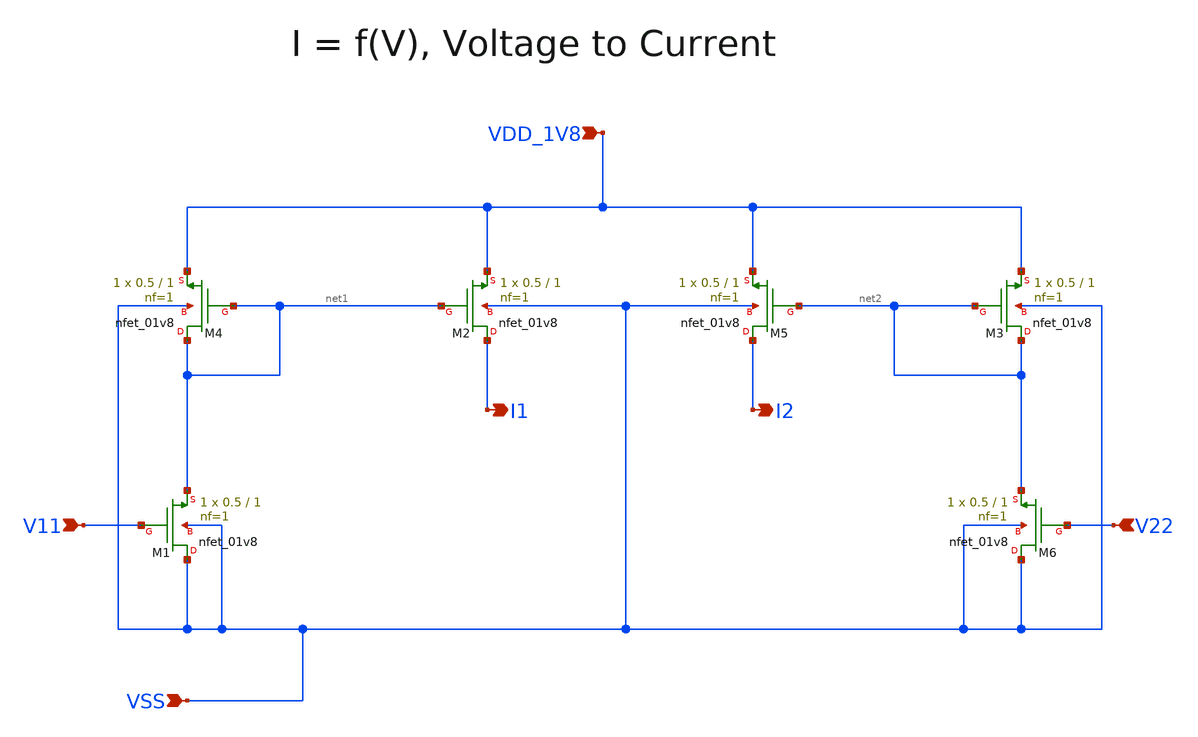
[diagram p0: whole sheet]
** sch_path: design/CNR_GR06_SKY130NM/CNR_GR06_V_to_I.sch
**.subckt CNR_GR06_V_to_I VDD_1V8 VSS I1 I2 V11 V22
*.ipin VDD_1V8
*.ipin VSS
*.opin I1
*.opin I2
*.ipin V11
*.ipin V22
XM1 VSS V11 net1 VSS sky130_fd_pr__nfet_01v8 L=1 W=0.5 nf=1 ad='int((nf+1)/2) * W/nf * 0.29' as='int((nf+2)/2) * W/nf * 0.29'
+ pd='2*int((nf+1)/2) * (W/nf + 0.29)' ps='2*int((nf+2)/2) * (W/nf + 0.29)' nrd='0.29 / W' nrs='0.29 / W'
+ sa=0 sb=0 sd=0 mult=1 m=1
XM2 I1 net1 VDD_1V8 VSS sky130_fd_pr__nfet_01v8 L=1 W=0.5 nf=1 ad='int((nf+1)/2) * W/nf * 0.29' as='int((nf+2)/2) * W/nf * 0.29'
+ pd='2*int((nf+1)/2) * (W/nf + 0.29)' ps='2*int((nf+2)/2) * (W/nf + 0.29)' nrd='0.29 / W' nrs='0.29 / W'
+ sa=0 sb=0 sd=0 mult=1 m=1
XM3 net2 net2 VDD_1V8 VSS sky130_fd_pr__nfet_01v8 L=1 W=0.5 nf=1 ad='int((nf+1)/2) * W/nf * 0.29' as='int((nf+2)/2) * W/nf * 0.29'
+ pd='2*int((nf+1)/2) * (W/nf + 0.29)' ps='2*int((nf+2)/2) * (W/nf + 0.29)' nrd='0.29 / W' nrs='0.29 / W'
+ sa=0 sb=0 sd=0 mult=1 m=1
XM4 net1 net1 VDD_1V8 VSS sky130_fd_pr__nfet_01v8 L=1 W=0.5 nf=1 ad='int((nf+1)/2) * W/nf * 0.29' as='int((nf+2)/2) * W/nf * 0.29'
+ pd='2*int((nf+1)/2) * (W/nf + 0.29)' ps='2*int((nf+2)/2) * (W/nf + 0.29)' nrd='0.29 / W' nrs='0.29 / W'
+ sa=0 sb=0 sd=0 mult=1 m=1
XM5 I2 net2 VDD_1V8 VSS sky130_fd_pr__nfet_01v8 L=1 W=0.5 nf=1 ad='int((nf+1)/2) * W/nf * 0.29' as='int((nf+2)/2) * W/nf * 0.29'
+ pd='2*int((nf+1)/2) * (W/nf + 0.29)' ps='2*int((nf+2)/2) * (W/nf + 0.29)' nrd='0.29 / W' nrs='0.29 / W'
+ sa=0 sb=0 sd=0 mult=1 m=1
XM6 VSS V22 net2 VSS sky130_fd_pr__nfet_01v8 L=1 W=0.5 nf=1 ad='int((nf+1)/2) * W/nf * 0.29' as='int((nf+2)/2) * W/nf * 0.29'
+ pd='2*int((nf+1)/2) * (W/nf + 0.29)' ps='2*int((nf+2)/2) * (W/nf + 0.29)' nrd='0.29 / W' nrs='0.29 / W'
+ sa=0 sb=0 sd=0 mult=1 m=1
**.ends
.end
